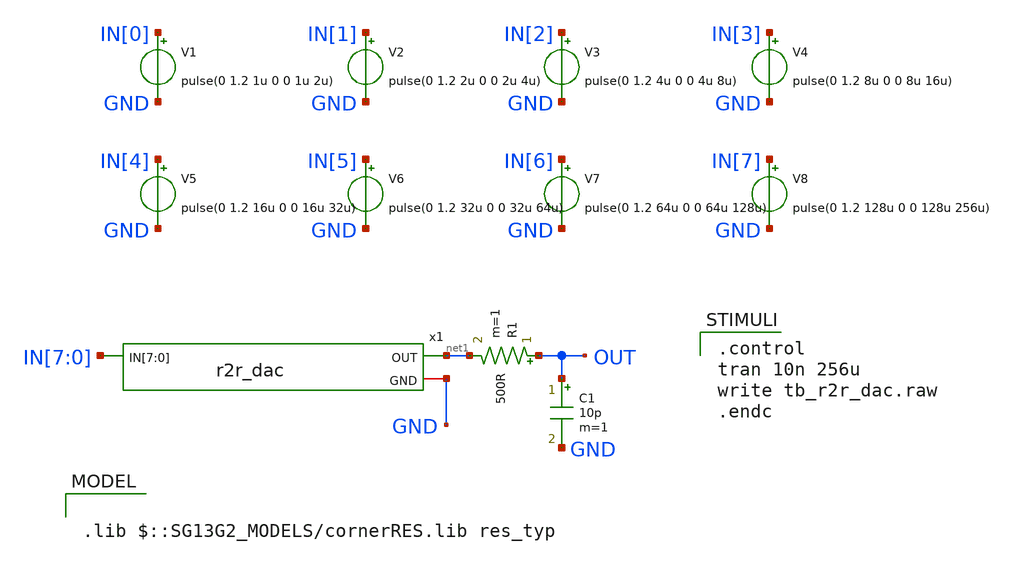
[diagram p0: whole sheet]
** sch_path: xschem/tb_r2r_dac.sch
**.subckt tb_r2r_dac
x1 IN[7] IN[6] IN[5] IN[4] IN[3] IN[2] IN[1] IN[0] net1 GND r2r_dac
V4 IN[3] GND pulse(0 1.2 8u 0 0 8u 16u)
V3 IN[2] GND pulse(0 1.2 4u 0 0 4u 8u)
V2 IN[1] GND pulse(0 1.2 2u 0 0 2u 4u)
V1 IN[0] GND pulse(0 1.2 1u 0 0 1u 2u)
R1 OUT net1 500R m=1
C1 OUT GND 10p m=1
V8 IN[7] GND pulse(0 1.2 128u 0 0 128u 256u)
V7 IN[6] GND pulse(0 1.2 64u 0 0 64u 128u)
V6 IN[5] GND pulse(0 1.2 32u 0 0 32u 64u)
V5 IN[4] GND pulse(0 1.2 16u 0 0 16u 32u)
**** begin user architecture code

.control
tran 10n 256u
write tb_r2r_dac.raw
.endc


.lib $::SG13G2_MODELS/cornerRES.lib res_typ

**** end user architecture code
**.ends

* expanding   symbol:  r2r_dac.sym # of pins=3
** sym_path: xschem/r2r_dac.sym
** sch_path: xschem/r2r_dac.sch
.subckt r2r_dac IN[7] IN[6] IN[5] IN[4] IN[3] IN[2] IN[1] IN[0] OUT GND
*.ipin IN[7],IN[6],IN[5],IN[4],IN[3],IN[2],IN[1],IN[0]
*.iopin GND
*.opin OUT
XR0a IN[0] net1 sub! rhigh w=1.0e-6 l=6.0e-6 m=1 b=0 mm_ok=1
XR0b net1 net3 sub! rhigh w=1.0e-6 l=6.0e-6 m=1 b=0 mm_ok=1
XR1c net4 net3 sub! rhigh w=1.0e-6 l=6.0e-6 m=1 b=0 mm_ok=1
XR0c net3 net2 sub! rhigh w=1.0e-6 l=6.0e-6 m=1 b=0 mm_ok=1
XR0d net2 GND sub! rhigh w=1.0e-6 l=6.0e-6 m=1 b=0 mm_ok=1
XR1a IN[1] net5 sub! rhigh w=1.0e-6 l=6.0e-6 m=1 b=0 mm_ok=1
XR1b net5 net4 sub! rhigh w=1.0e-6 l=6.0e-6 m=1 b=0 mm_ok=1
XR2c net6 net4 sub! rhigh w=1.0e-6 l=6.0e-6 m=1 b=0 mm_ok=1
XR2a IN[2] net7 sub! rhigh w=1.0e-6 l=6.0e-6 m=1 b=0 mm_ok=1
XR2b net7 net6 sub! rhigh w=1.0e-6 l=6.0e-6 m=1 b=0 mm_ok=1
XR3c net8 net6 sub! rhigh w=1.0e-6 l=6.0e-6 m=1 b=0 mm_ok=1
XR3a IN[3] net9 sub! rhigh w=1.0e-6 l=6.0e-6 m=1 b=0 mm_ok=1
XR3b net9 net8 sub! rhigh w=1.0e-6 l=6.0e-6 m=1 b=0 mm_ok=1
XR4c net10 net8 sub! rhigh w=1.0e-6 l=6.0e-6 m=1 b=0 mm_ok=1
XR4a IN[4] net11 sub! rhigh w=1.0e-6 l=6.0e-6 m=1 b=0 mm_ok=1
XR4b net11 net10 sub! rhigh w=1.0e-6 l=6.0e-6 m=1 b=0 mm_ok=1
XR5c net12 net10 sub! rhigh w=1.0e-6 l=6.0e-6 m=1 b=0 mm_ok=1
XR5a IN[5] net13 sub! rhigh w=1.0e-6 l=6.0e-6 m=1 b=0 mm_ok=1
XR5b net13 net12 sub! rhigh w=1.0e-6 l=6.0e-6 m=1 b=0 mm_ok=1
XR6c net14 net12 sub! rhigh w=1.0e-6 l=6.0e-6 m=1 b=0 mm_ok=1
XR6a IN[6] net15 sub! rhigh w=1.0e-6 l=6.0e-6 m=1 b=0 mm_ok=1
XR6b net15 net14 sub! rhigh w=1.0e-6 l=6.0e-6 m=1 b=0 mm_ok=1
XR7c OUT net14 sub! rhigh w=1.0e-6 l=6.0e-6 m=1 b=0 mm_ok=1
XR7a IN[7] net16 sub! rhigh w=1.0e-6 l=6.0e-6 m=1 b=0 mm_ok=1
XR7b net16 OUT sub! rhigh w=1.0e-6 l=6.0e-6 m=1 b=0 mm_ok=1
.ends

.end
